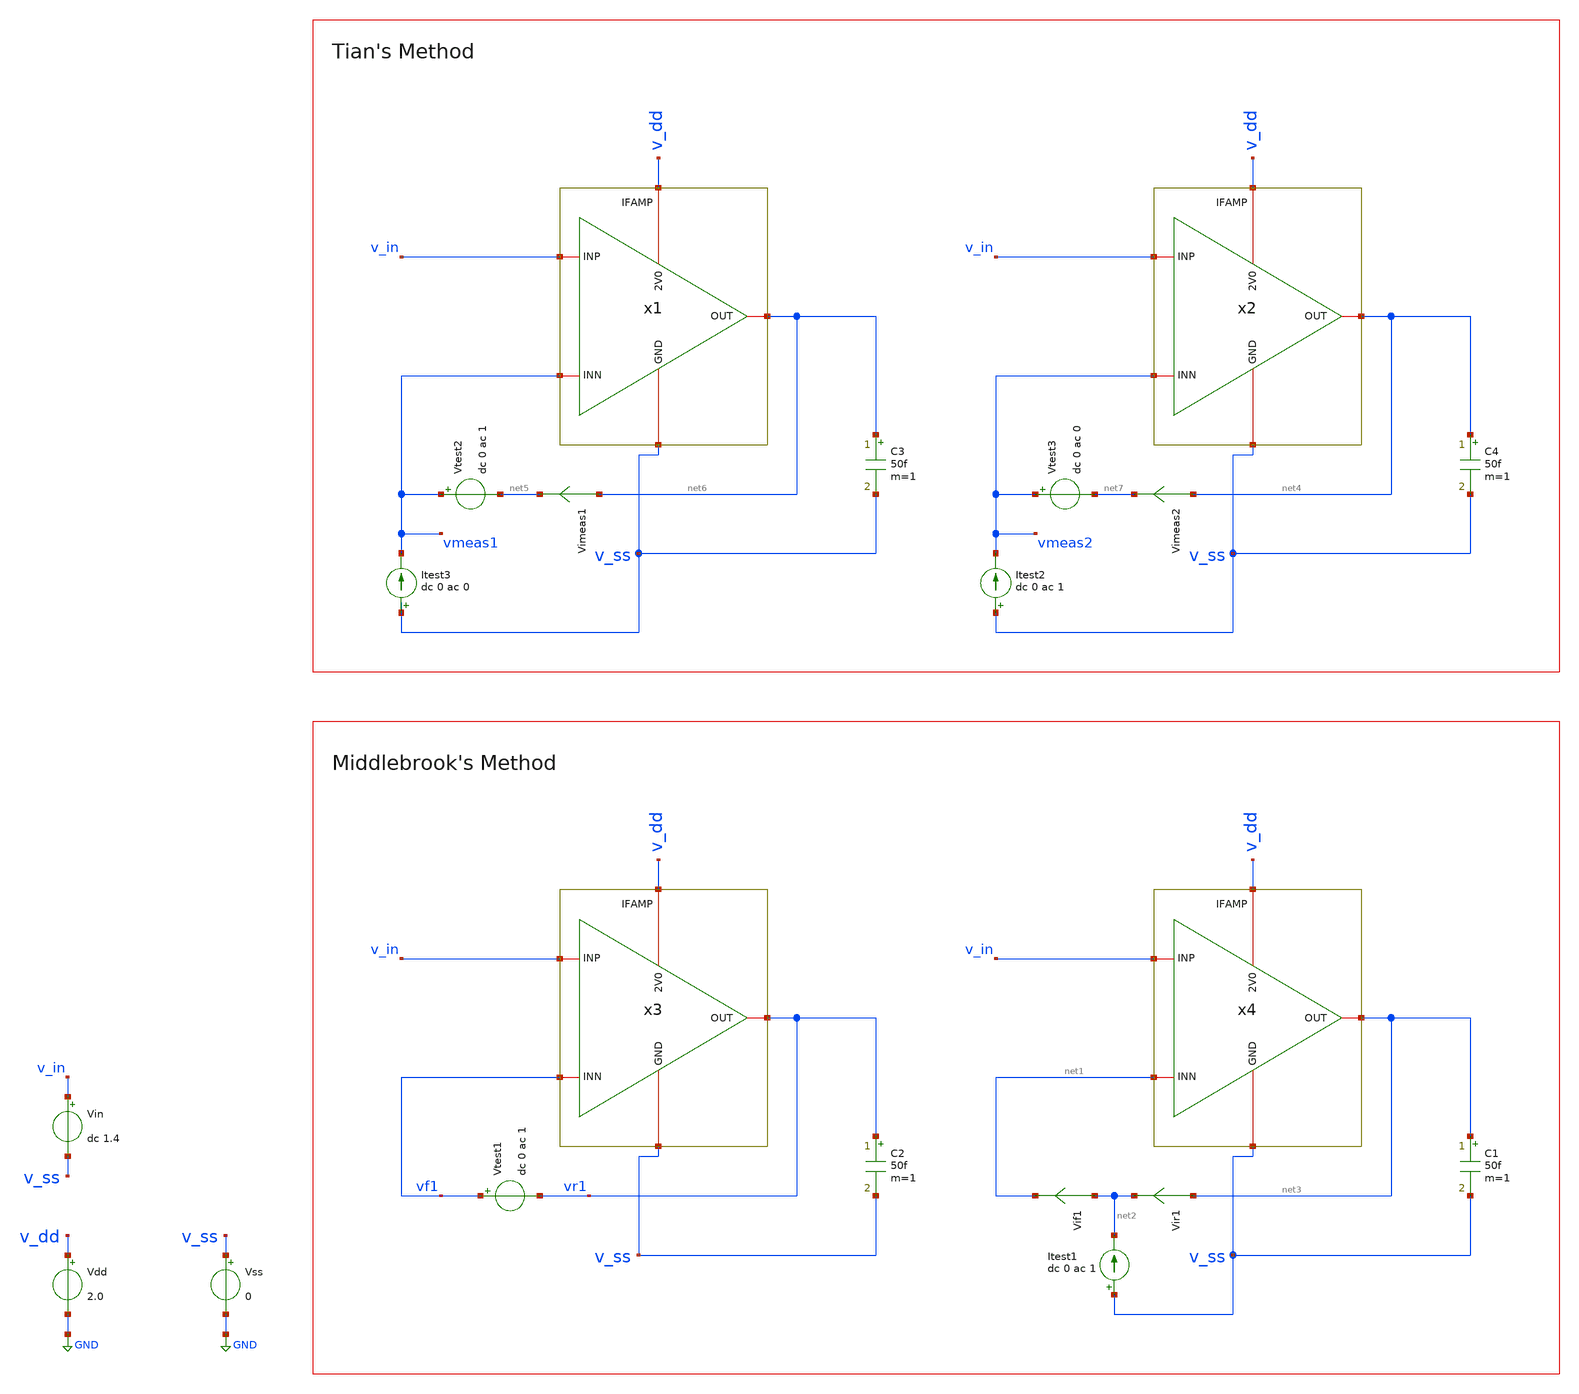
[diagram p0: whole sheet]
** sch_path: mWATTBAT/design_data/xschem/IFAMP_STAB_NGSPICE.sch
* (c) 2024 H. Pretl, S. Dorrer, Apache-2.0 license
**.subckt IFAMP_STAB_NGSPICE
Vdd v_dd GND 2.0
Vss v_ss GND 0
Vin v_in v_ss dc 1.4
C2 vr1 v_ss 50f m=1
Vtest1 vf1 vr1 dc 0 ac 1
C1 net3 v_ss 50f m=1
Vir1 net3 net2 0
.save i(vir1)
Vif1 net2 net1 0
.save i(vif1)
Itest1 v_ss net2 dc 0 ac 1
C3 net6 v_ss 50f m=1
C4 net4 v_ss 50f m=1
Itest3 v_ss vmeas1 dc 0 ac 0
Vtest2 vmeas1 net5 dc 0 ac 1
Vimeas1 net6 net5 0
.save i(vimeas1)
Itest2 v_ss vmeas2 dc 0 ac 1
Vtest3 vmeas2 net7 dc 0 ac 0
Vimeas2 net4 net7 0
.save i(vimeas2)
x1 v_dd v_in vmeas1 net6 v_ss IFAMP
x2 v_dd v_in vmeas2 net4 v_ss IFAMP
x3 v_dd v_in vf1 vr1 v_ss IFAMP
x4 v_dd v_in net1 net3 v_ss IFAMP
**** begin user architecture code

.lib cornerMOSlv.lib mos_tt
.lib cornerRES.lib res_typ



.param temp=27
.options savecurrents reltol=1e-3 abstol=1e-12 gmin=1e-15
.control
save all

* Operating Point Analysis
op
remzerovec
write ota-improved_tb-loopgain.raw
set appendwrite

* AC Analysis
ac dec 101 1 100G
remzerovec
write ota-improved_tb-loopgain.raw
set appendwrite

* Middlebrook's Method
let tv=-v(vr1)/v(vf1)
let ti=-i(vir1)/i(vif1)
let tmb=(tv*ti - 1)/(tv + ti + 2)

plot db(tmb) ylabel 'Magnitude - Middlebrook'
plot 180-180/pi*cphase(tmb) ylabel 'Phase Margin- Middlebrook'

* Tian's Method
* vtest=0, itest=1:
let A=i(Vimeas2)
let C=v(vmeas2)

* vtest=1, itest=0:
let B=i(Vimeas1)
let D=v(vmeas1)
let ttian=(A*D-B*C-A)/(2*(B*C-A*D)+A-D+1)

plot db(ttian) ylabel 'Magnitude - Tian'
plot 180-180/pi*cphase(ttian) ylabel 'Phase Margin- Tian'

* Middlebrook vs. Tian
plot db(tmb) db(ttian) ylabel 'Magnitude'
plot 180/pi*cphase(tmb) 180/pi*cphase(ttian) ylabel 'Phase'

write ota-improved_tb-loopgain.raw

*quit
.endc


**** end user architecture code
**.ends

* expanding   symbol:  /foss/designs/mWATTBAT/design_data/xschem/IFAMP.sym # of pins=5
** sym_path: mWATTBAT/design_data/xschem/IFAMP.sym
** sch_path: mWATTBAT/design_data/xschem/IFAMP.sch
.subckt IFAMP 2V0 INP INN OUT GND
*.iopin INP
*.iopin INN
*.iopin OUT
*.iopin 2V0
*.iopin GND
XM1 vs_1c INP vs_1_2 2V0 sg13_lv_pmos w=29u l=0.25u ng=29 m=1 mm_ok=1
XM2 vs_2c INN vs_1_2 2V0 sg13_lv_pmos w=29u l=0.25u ng=29 m=1 mm_ok=1
XM1C vg_3_4 vg_1c_2c vs_1c 2V0 sg13_lv_pmos w=4u l=0.25u ng=20 m=1 mm_ok=1
XM2C OUT1 vg_1c_2c vs_2c 2V0 sg13_lv_pmos w=4u l=0.25u ng=20 m=1 mm_ok=1
XM3C vg_3_4 vg_3c_4c vs_3c GND sg13_lv_nmos w=0.5u l=1u ng=2 m=1 mm_ok=1
XM4C OUT1 vg_3c_4c vs_4c GND sg13_lv_nmos w=0.5u l=1u ng=2 m=1 mm_ok=1
XM3 vs_3c vg_3_4 GND GND sg13_lv_nmos w=0.5u l=1u ng=1 m=1 mm_ok=1
XM4 vs_4c vg_3_4 GND GND sg13_lv_nmos w=0.5u l=1u ng=1 m=1 mm_ok=1
XM5 vs_1_2 vg_5_6 2V0 2V0 sg13_lv_pmos w=26.5u l=5u ng=20 m=1 mm_ok=1
XM6 vg_5_6 vg_5_6 2V0 2V0 sg13_lv_pmos w=13.25u l=5u ng=10 m=1 mm_ok=1
XM7 OUT OUT1 GND GND sg13_hv_nmos w=8.4u l=0.6u ng=14 m=1 mm_ok=1
XM8 OUT OUT1 2V0 2V0 sg13_hv_pmos w=0.6u l=0.6u ng=1 m=1 mm_ok=1
XM9 vg_3c_4c vg_3c_4c vs_1_2 2V0 sg13_lv_pmos w=0.84u l=6u ng=4 m=1 mm_ok=1
XM10 vg_3c_4c vg_3c_4c vg_1c_2c GND sg13_lv_nmos w=15u l=5u ng=20 m=1 mm_ok=1
XM11 vg_1c_2c vg_1c_2c GND GND sg13_lv_nmos w=0.4u l=6u ng=2 m=1 mm_ok=1
XM13 vg_13 vg_13 GND GND sg13_lv_nmos w=1.6u l=5u ng=8 m=1 mm_ok=1
XM12 vg_5_6 vg_5_6 vg_13 GND sg13_lv_nmos w=1.6u l=5u ng=8 m=1 mm_ok=1
**** begin user architecture code



**** end user architecture code
**** begin user architecture code



.lib $::SG13G2_MODELS/cornerMOSlv.lib mos_tt
.lib $::SG13G2_MODELS/cornerMOShv.lib mos_tt
.lib $::SG13G2_MODELS/cornerRES.lib res_typ
.lib $::SG13G2_MODELS/cornerHBT.lib hbt_typ



**** end user architecture code
XM13D VSS vg_13 VSS VSS sg13_lv_nmos w=2.6u l=5u ng=13 m=2 mm_ok=1
XM12D VSS vg_5_6 VSS VSS sg13_lv_nmos w=2.6u l=5u ng=13 m=2 mm_ok=1
XM6D VDD vg_5_6 VDD VDD sg13_lv_pmos w=15.9u l=5u ng=12 m=2 mm_ok=1
XM5D VDD vs_1_2 VDD VDD sg13_lv_pmos w=9.275u l=5u ng=7 m=2 mm_ok=1
XM11D VSS vg_1c_2c VSS VSS sg13_lv_nmos w=2.6u l=6u ng=13 m=2 mm_ok=1
XM9D VDD vg_3c_4c VDD VDD sg13_lv_pmos w=2.52u l=6u ng=12 m=2 mm_ok=1
XM10D VSS vg_3c_4c VSS VSS sg13_lv_nmos w=5.25u l=5u ng=7 m=2 mm_ok=1
XM3CD VSS vg_3c_4c VSS VSS sg13_lv_nmos w=15.25u l=1u ng=61 m=1 mm_ok=1
XM3D VSS VSS VSS VSS sg13_lv_nmos w=0.5u l=1u ng=1 m=86 mm_ok=1
XM4CD VSS vg_3c_4c VSS VSS sg13_lv_nmos w=15.25u l=1u ng=61 m=1 mm_ok=1
XM1CD VDD vg_1c_2c VDD VDD sg13_lv_pmos w=22u l=0.25u ng=110 m=1 mm_ok=1
XM2CD VDD vg_1c_2c VDD VDD sg13_lv_pmos w=22u l=0.25u ng=110 m=1 mm_ok=1
XM1D VDD vs_1_2 VDD VDD sg13_lv_pmos w=115u l=0.25u ng=115 m=1 mm_ok=1
XM2D VDD vs_1_2 VDD VDD sg13_lv_pmos w=115u l=0.25u ng=115 m=1 mm_ok=1
XM4D VSS VSS VSS VSS sg13_lv_nmos w=0.5u l=1u ng=1 m=86 mm_ok=1
XM7D VSS VDD VSS VSS sg13_hv_nmos w=8.4u l=0.6u ng=14 m=56 mm_ok=1
XM8D VDD VSS VDD VDD sg13_hv_pmos w=0.6u l=0.6u ng=1 m=56 mm_ok=1
XR21 OUT OUT1 sub! rppd w=2.21e-6 l=10.0e-6 m=1 b=67 mm_ok=1
.ends

.GLOBAL GND
.end
